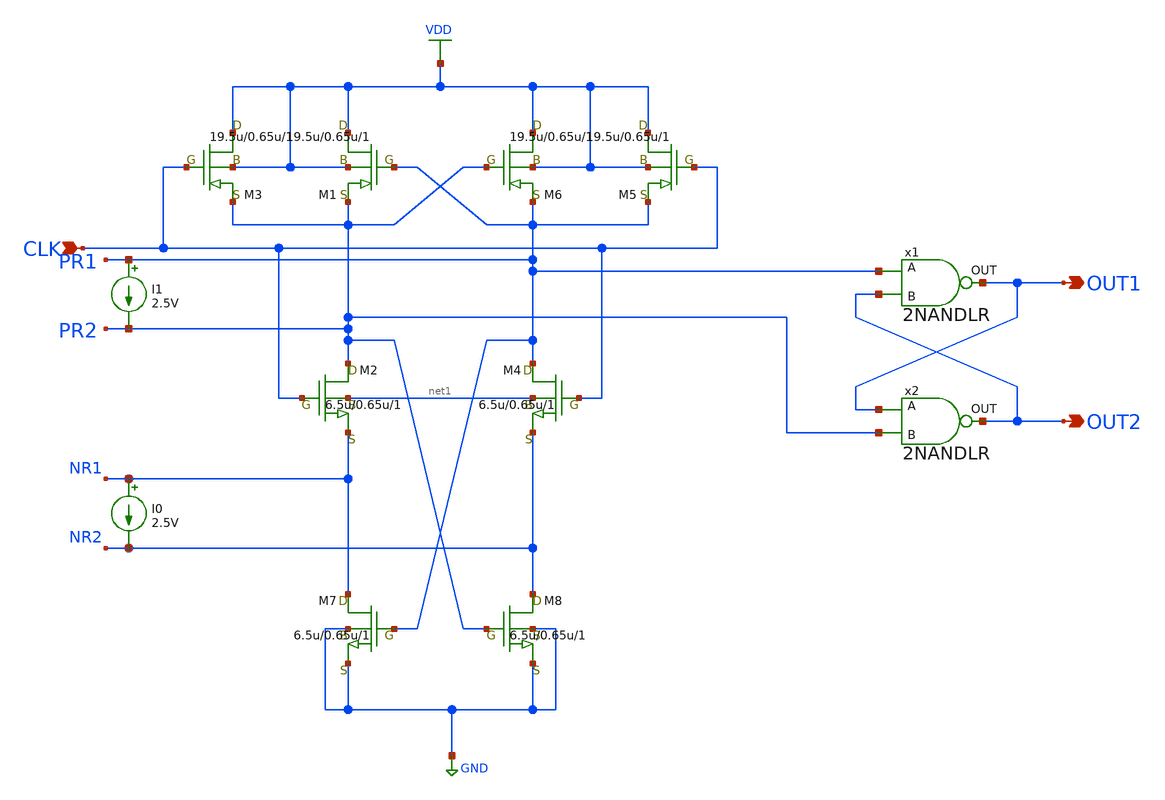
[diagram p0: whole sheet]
** sch_path: LR_hokari/LR_Work2/Wide-swing_clocked_comparatortest.sch
**.subckt Wide-swing_clocked_comparatortest CLK OUT1 OUT2
*.ipin CLK
*.opin OUT1
*.opin OUT2
M2 PR2 CLK NR1 net1 nch w=6.5u l=0.65u as=0 ps=0 ad=0 pd=0 m=1
M4 PR1 CLK NR2 net1 nch w=6.5u l=0.65u as=0 ps=0 ad=0 pd=0 m=1
M5 VDD CLK PR1 VDD pch w=19.5u l=0.65u as=0 ps=0 ad=0 pd=0 m=1
M6 VDD PR2 PR1 VDD pch w=19.5u l=0.65u as=0 ps=0 ad=0 pd=0 m=1
M7 NR1 PR1 GND GND nch w=6.5u l=0.65u as=0 ps=0 ad=0 pd=0 m=1
M8 NR2 PR2 GND GND nch w=6.5u l=0.65u as=0 ps=0 ad=0 pd=0 m=1
x1 PR1 OUT1 OUT2 2NANDLR
x2 OUT1 OUT2 PR2 2NANDLR
M1 VDD PR1 PR2 VDD pch w=19.5u l=0.65u as=0 ps=0 ad=0 pd=0 m=1
M3 VDD CLK PR2 VDD pch w=19.5u l=0.65u as=0 ps=0 ad=0 pd=0 m=1
I0 NR1 NR2 2.5V
I1 PR1 PR2 2.5V
**** begin user architecture code



.inc /home/tororo/LR/T_mos_model.sp

VVDD VDD 0 DC 3.3

*VINP INP 0 pwl (0 0 25n 0 26n 3.3 75n 3.3 76n 0.2 125n 0.2 126n 3.1 175n 3.1 176n 0.4 225n 0.4 226n
*+ 2.9 275n 2.9 276n 0.6 325n 0.6 326n 2.7 375n 2.7 376n 0.8 425n 0.8 426n 2.5 475n 2.5 476n 1.0 525n 1.0
*+ 526n 2.3 575n 2.3 576n 1.2 625n 1.2
*+ 626n 2.1 675n 2.1 +676n 1.4 725n 1.4 726n 1.9 775n 1.9 776n 1.6 825n 1.6 826n 1.7 875n 1.7 )
*VINP INP 0 pwl (0 0 25n 0 26n 1.7 75n 1.7 76n 1.6 125n 1.6 126n 1.68 175n 1.68 176n 1.62 225n 1.62
*+ 226n 1.66 275n 1.66 276n 1.64 325n 1.64 326n 1.655 375n 1.655 376n 1.645 425n 1.645 426n 1.651 475n
*+ 1.651 476n 1.649 525n 1.649 526n 1.6501 575n 1.6501 576n 1.6499 625n 1.6499 626n 1.65001 675n 1.65001
*+ 676n 1.64999 725n 1.6499 726n 1.9 775n 1.9 776n 1.6 825n 1.6 826n 1.7 875n 1.7)
*VINP INP 0 pwl (0 2.15 25n 2.15 26n 1.15 75n 1.15 76n 1.95 125n 1.95 126n 1.35 175n 1.35)
*VINP INP 0 pwl (0 1.85 25n 1.85 26n 1.45 75n 1.45 76n 1.83 125n 1.83 126n 1.47 175n 1.47)

*VREF REF 0 DC 1.65

*VCLK CLK 0 pulse(0 3.3 0 1p 1p 12.5n 50n)
VCLK CLK 0 pulse(0 3.3 0n 1n 1n 12.5n 25n)

.control
tran 1n 875n

*meas tran delayIN1 find time WHEN v(CLK)=0.9 RISE=3
*meas tran delayOUT find time WHEN v(OUT1)=0.9 FALL=2
*let delay1 = delayOUT - delayIN1
*echo tpHL = $&delay1

*meas tran delayIN1 find time WHEN v(CLK)=0.9 RISE=4
*meas tran delayOUT find time WHEN v(OUT1)=0.9 RISE=2
*let delay2 = delayOUT - delayIN1
*echo tpLH = $&delay2


write Wide-swing_clocked_comparatortest.raw

.endc

**** end user architecture code
**.ends

* expanding   symbol:  LR_Work2/symbol/2NANDLR.sym # of pins=3
** sym_path: LR_hokari/LR_Work2/symbol/2NANDLR.sym
** sch_path: LR_hokari/LR_Work2/symbol/2NANDLR.sch
.subckt 2NANDLR A OUT B
*.ipin A
*.ipin B
*.opin OUT
M1 OUT A net1 GND nch w=3.5u l=3.5u as=0 ps=0 ad=0 pd=0 m=1
M2 OUT B VDD VDD pch w=10.5u l=3.5u as=0 ps=0 ad=0 pd=0 m=1
M3 OUT A VDD VDD pch w=10.5u l=3.5u as=0 ps=0 ad=0 pd=0 m=1
M4 net1 B GND GND nch w=3.5u l=10.5u as=0 ps=0 ad=0 pd=0 m=1
.ends

.GLOBAL VDD
.GLOBAL GND
.end
